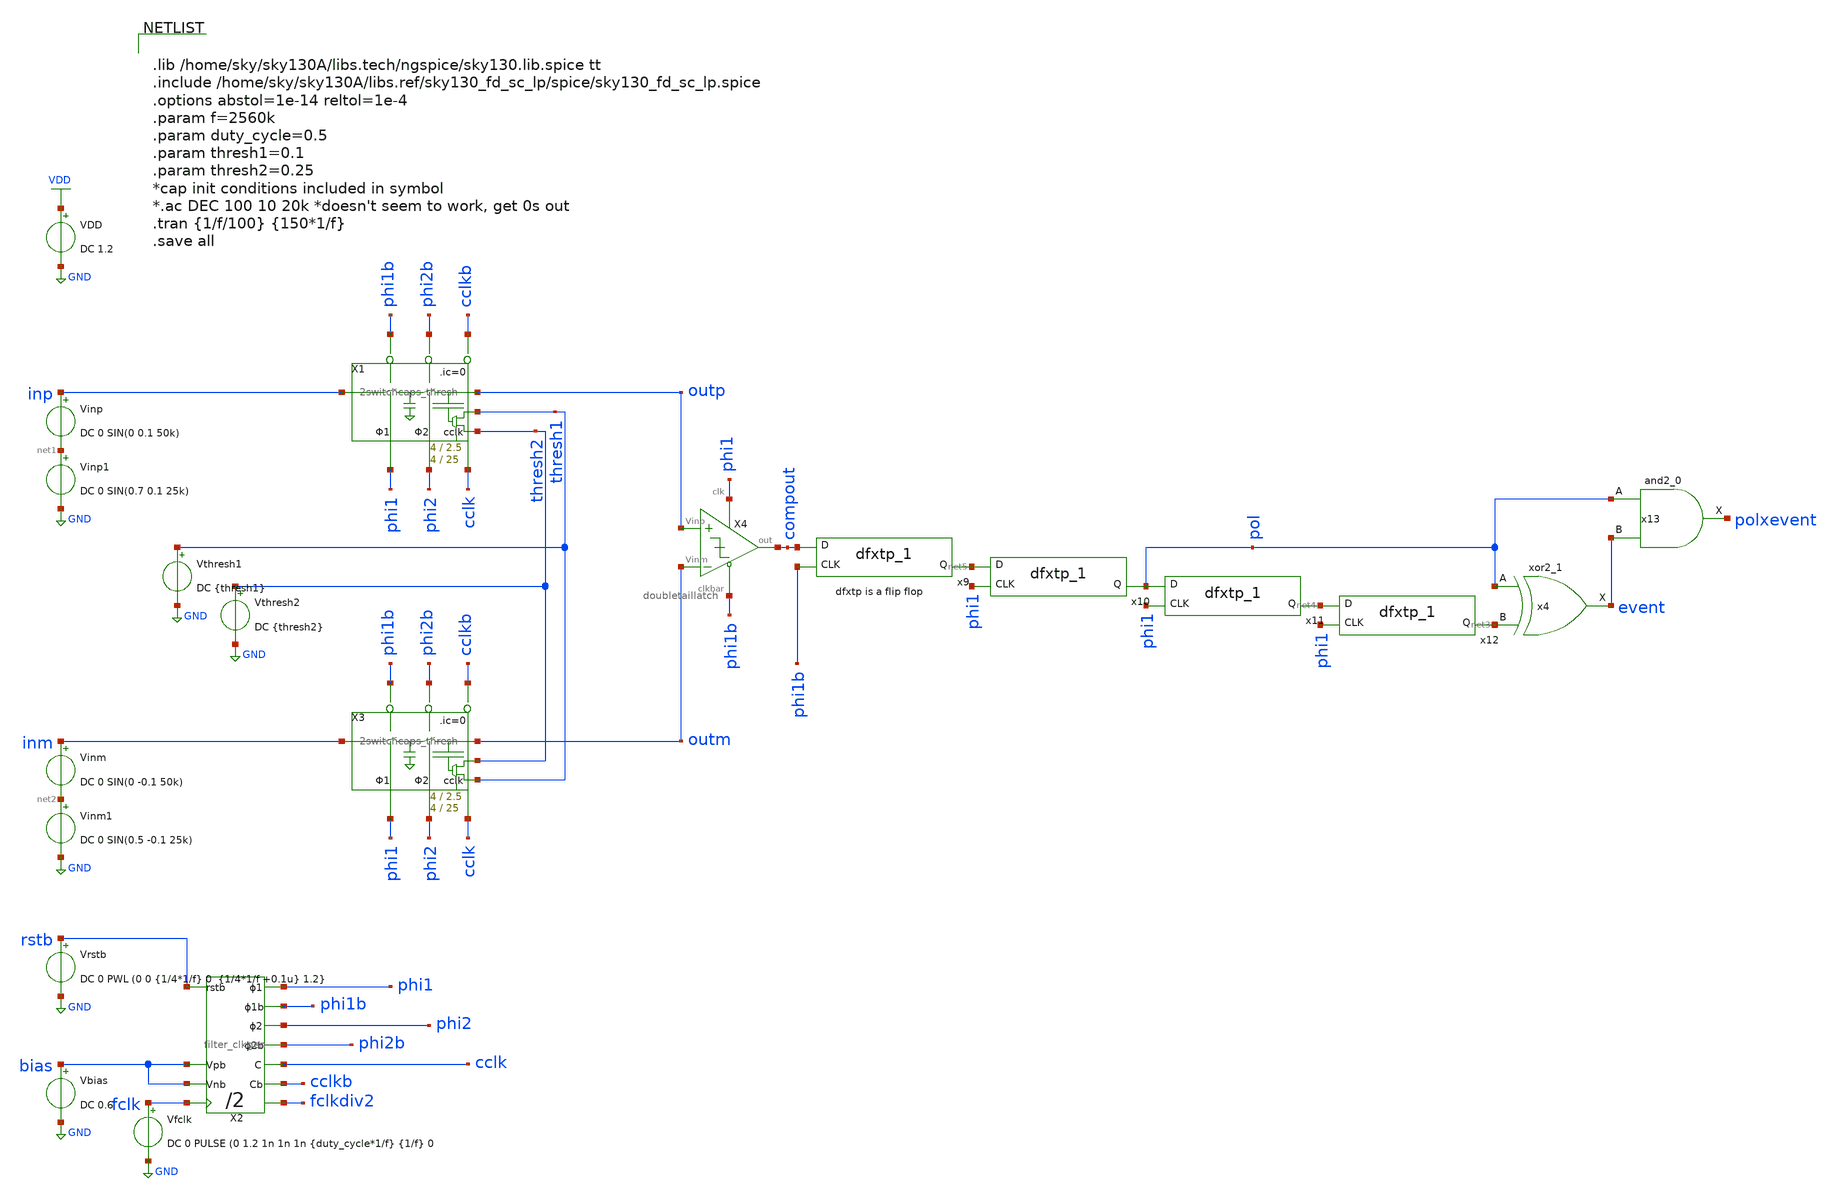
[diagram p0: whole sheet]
** sch_path: xschem/comparator/2switchcaps_thresh_diff_tb.sch
**.subckt 2switchcaps_thresh_diff_tb
Vinp inp net1 DC 0 SIN(0 0.1 50k)
VDD VDD GND DC 1.2
Vfclk fclk GND DC 0 PULSE (0 1.2 1n 1n 1n {duty_cycle*1/f} {1/f} 0
X1 inp outp phi2 phi1 phi1b phi2b thresh2 cclk thresh1 cclkb 2switchcaps_thresh Wcap1=4 Lcap1=2.5
+ Wcap2=4 Lcap2=25
X2 rstb fclk phi2b phi2 phi1b phi1 cclkb cclk fclkdiv2 bias bias filter_clkgen
Vbias bias GND DC 0.6
Vthresh1 thresh1 GND DC {thresh1}
Vthresh2 thresh2 GND DC {thresh2}
Vrstb rstb GND DC 0 PWL (0 0 {1/4*1/f} 0 {1/4*1/f +0.1u} 1.2}
Vinm inm net2 DC 0 SIN(0 -0.1 50k)
X3 inm outm phi2 phi1 phi1b phi2b thresh1 cclk thresh2 cclkb 2switchcaps_thresh Wcap1=4 Lcap1=2.5 Wcap2=4 Lcap2=25
X4 outp outm compout phi1 phi1b doubletaillatch
Vinp1 net1 GND DC 0 SIN(0.7 0.1 25k)
Vinm1 net2 GND DC 0 SIN(0.5 -0.1 25k)
x4 pol net3 GND GND VDD VDD event sky130_fd_sc_lp__xor2_1
x11 phi1 pol gnd gnd vdd vdd net4 sky130_fd_sc_lp__dfxtp_1
x12 phi1 net4 gnd gnd vdd vdd net3 sky130_fd_sc_lp__dfxtp_1
x9 phi1b compout gnd gnd vdd vdd net5 sky130_fd_sc_lp__dfxtp_1
x10 phi1 net5 gnd gnd vdd vdd pol sky130_fd_sc_lp__dfxtp_1
x13 pol event GND GND VDD VDD polxevent sky130_fd_sc_lp__and2_0
**** begin user architecture code


.lib /home/sky/sky130A/libs.tech/ngspice/sky130.lib.spice tt
.include /home/sky/sky130A/libs.ref/sky130_fd_sc_lp/spice/sky130_fd_sc_lp.spice
.options abstol=1e-14 reltol=1e-4
.param f=2560k
.param duty_cycle=0.5
.param thresh1=0.1
.param thresh2=0.25
*cap init conditions included in symbol
*.ac DEC 100 10 20k *doesn't seem to work, get 0s out
.tran {1/f/100} {150*1/f}
.save all


**** end user architecture code
**.ends
.GLOBAL GND
.GLOBAL VDD
.end
